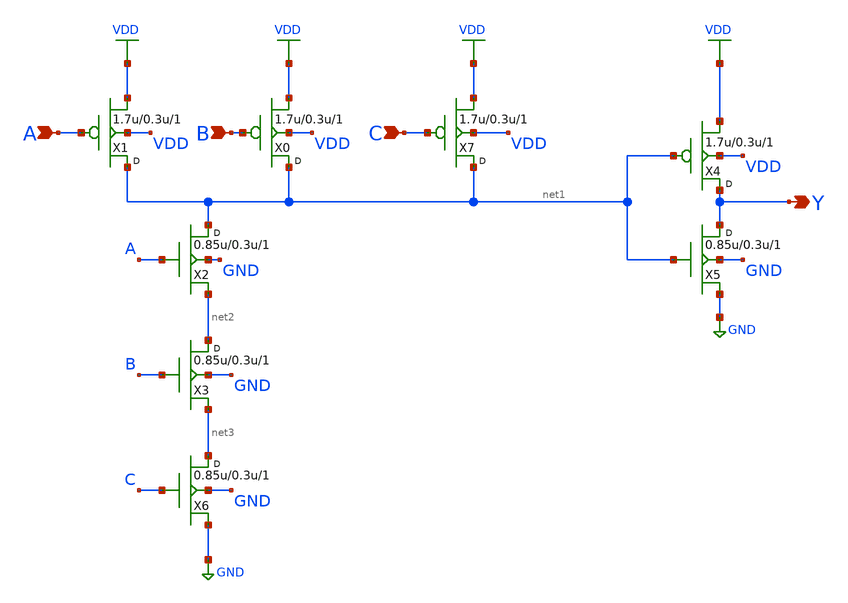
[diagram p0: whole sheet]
** sch_path: designs/libs/core_digital/gf180mcu_osu_sc_gp12t3v3/cells/and3/gf180mcu_osu_sc_gp12t3v3_and3_1.sch
**.subckt gf180mcu_osu_sc_gp12t3v3_and3_1 A B Y C
*.ipin A
*.ipin B
*.opin Y
*.ipin C
X1 net1 A VDD VDD pfet_03v3 w=1.7u l=0.3u m=1
X0 net1 B VDD VDD pfet_03v3 w=1.7u l=0.3u m=1
X2 net1 A net2 GND nfet_03v3 w=0.85u l=0.3u m=1
X3 net2 B net3 GND nfet_03v3 w=0.85u l=0.3u m=1
X4 Y net1 VDD VDD pfet_03p3 w=1.7u l=0.3u m=1
X5 Y net1 GND GND nfet_03p3 w=0.85u l=0.3u m=1
X6 net3 C GND GND nfet_03v3 w=0.85u l=0.3u m=1
X7 net1 C VDD VDD pfet_03v3 w=1.7u l=0.3u m=1
**.ends
.GLOBAL VDD
.GLOBAL GND
.end
